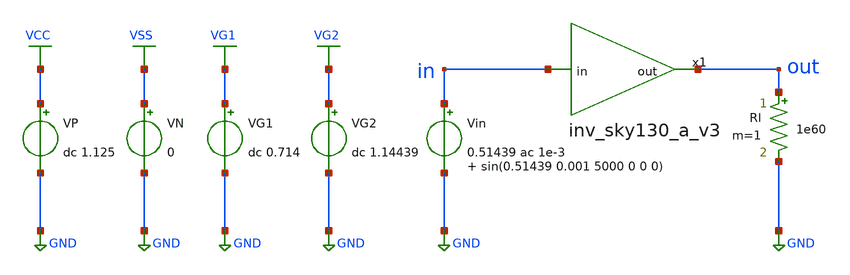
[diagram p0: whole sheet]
** sch_path: Amplifier_Inv/xschem/v3/tb_inv_sky130_a_v3.sch
* StefanSchippers/xschem_sky130/sky130_tests/not.sch:
* Copyright 2021 Stefan Frederik Schippers
* Licensed under the Apache License, Version 2.0 (the "License");
**.subckt tb_inv_sky130_a_v3
VN VSS GND 0
VP VCC GND dc 1.125
.save i(vp)
Vin in GND 0.51439 ac 1e-3 sin(0.51439 0.001 5000 0 0 0)
.save i(vin)
Rl out GND 1e60 m=1
VG2 VG2 GND dc 1.14439
VG1 VG1 GND dc 0.714
.save i(vg1)
x1 out in inv_sky130_a_v3
**** begin user architecture code

** opencircuitdesign pdks install
.lib $::SKYWATER_MODELS/sky130.lib.spice tt



.control

  op
  save all
  let gmn = @m.x1.x1.xm1.msky130_fd_pr__nfet_01v8[gm]
  let gmp = @m.x1.x1.xm2.msky130_fd_pr__pfet_01v8[gm]
  let gdsn = @m.x1.x1.xm1.msky130_fd_pr__nfet_01v8[gds]
  let gdsp = @m.x1.x1.xm2.msky130_fd_pr__pfet_01v8[gds]
  let cgsn = @m.x1.x1.xm1.msky130_fd_pr__nfet_01v8[cgs]
  let cgsp = @m.x1.x1.xm2.msky130_fd_pr__pfet_01v8[cgs]
  let cgdn = @m.x1.x1.xm1.msky130_fd_pr__nfet_01v8[cgd]
  let cgdp = @m.x1.x1.xm2.msky130_fd_pr__pfet_01v8[cgd]
  write tb_inv_sky130_a_op_v3.raw gmn gmp gdsn gdsp cgsn cgsp cgdn cgdp

  ac dec 1000 1 1e8
  save all
  let gain = db(v(out)/v(in))
  let gain_vs1 = db(v(x1.vs1)/v(in))
  let phase = phase(v(out)/v(in))
  write tb_inv_sky130_a_AC_v3.raw gain gain_vs1

  noise v(out) Vin dec 1000 300 10k 10
  save all
  write tb_inv_sky130_a_noise_v3.raw

  noise v(out) Vin dec 1000 300 10k
  save all
  setplot noise1
  write tb_inv_sky130_a_noise_spectrum_v3.raw

  dc Vin 0 1.125 0.00001
  save all v(out) v(x1.vg1) v(x1.vg2) v(x1.vs1) v(x1.vd1)
  write tb_inv_sky130_a_DC_v3.raw v(out) v(x1.vg1) v(x1.vg2) v(x1.vs1) v(x1.vd1)

  tran 0.1u 4m
  save all
  let pw_in = i(Vin)*v(in)
  let pw_vcc = i(Vp)*1.125
  let pw_vg1 = i(Vg1)*0.64866
  let pw_vg2 = i(Vg2)*1.07866
  let pw_total = pw_in+pw_vcc
  meas tran avg_pw_total AVG pw_total FROM=0 TO=2m
  meas tran avg_pw_in AVG pw_in FROM=0 TO=2m
  meas tran avg_pw_vcc AVG pw_vcc FROM=0 TO=2m
  write tb_inv_sky130_a_tran_v3.raw v(in) v(out) v(x1.vd1) v(x1.vs1) v(vg1) v(vg2) avg_pw_total

  exit 0

.endc


**** end user architecture code
**.ends

* expanding   symbol:  v3/inv_sky130_a_v3.sym # of pins=2
** sym_path: Amplifier_Inv/xschem/v3/inv_sky130_a_v3.sym
** sch_path: Amplifier_Inv/xschem/v3/inv_sky130_a_v3.sch
.subckt inv_sky130_a_v3 out in
*.ipin in
*.opin out
x1 VS1 VD1 VCC VSS not W_N=250 L_N=1 W_P=200 L_P=0.25 m=1
XC1 in VD1 sky130_fd_pr__cap_mim_m3_1 W=26 L=26 MF=1 m=1
XM1 VD1 VG1 VS1 GND sky130_fd_pr__nfet_01v8 L=0.15 W=0.5 nf=1 ad='int((nf+1)/2) * W/nf * 0.29' as='int((nf+2)/2) * W/nf * 0.29'
+ pd='2*int((nf+1)/2) * (W/nf + 0.29)' ps='2*int((nf+2)/2) * (W/nf + 0.29)' nrd='0.29 / W' nrs='0.29 / W'
+ sa=0 sb=0 sd=0 mult=1 m=1
XM2 VS1 VG2 out GND sky130_fd_pr__nfet_01v8 L=0.15 W=0.5 nf=1 ad='int((nf+1)/2) * W/nf * 0.29' as='int((nf+2)/2) * W/nf * 0.29'
+ pd='2*int((nf+1)/2) * (W/nf + 0.29)' ps='2*int((nf+2)/2) * (W/nf + 0.29)' nrd='0.29 / W' nrs='0.29 / W'
+ sa=0 sb=0 sd=0 mult=1 m=1
XC2 out GND sky130_fd_pr__cap_mim_m3_1 W=50 L=50 MF=1 m=1
.ends


* expanding   symbol:  sky130_tests/not.sym # of pins=2
** sym_path: sky130_tests/not.sym
** sch_path: sky130_tests/not.sch
.subckt not y a VCCPIN VSSPIN     W_N=1 L_N=0.15 W_P=2 L_P=0.15
*.opin y
*.ipin a
XM1 DN a VSSPIN VSSPIN sky130_fd_pr__nfet_01v8 L=L_N W=W_N nf=1 ad='int((1 + 1)/2) * W_N / 1 * 0.29'
+ as='int((1 + 2)/2) * W_N / 1 * 0.29' pd='2*int((1 + 1)/2) * (W_N / 1 + 0.29)' ps='2*int((1 + 2)/2) * (W_N / 1 + 0.29)'
+ nrd='0.29 / W_N ' nrs='0.29 / W_N ' sa=0 sb=0 sd=0 mult=1 m=1
XM2 DP a VCCPIN VCCPIN sky130_fd_pr__pfet_01v8 L=L_P W=W_P nf=1 ad='int((nf+1)/2) * W/nf * 0.29' as='int((nf+2)/2) * W/nf * 0.29'
+ pd='2*int((nf+1)/2) * (W/nf + 0.29)' ps='2*int((nf+2)/2) * (W/nf + 0.29)' nrd='0.29 / W' nrs='0.29 / W'
+ sa=0 sb=0 sd=0 mult=1 m=1
Vmeas DP y 0
.save i(vmeas)
Vmeas1 y DN 0
.save i(vmeas1)
.save v(dp)
.save v(dn)
.ends

.GLOBAL GND
.GLOBAL VSS
.GLOBAL VCC
.GLOBAL VG2
.GLOBAL VG1
.end
